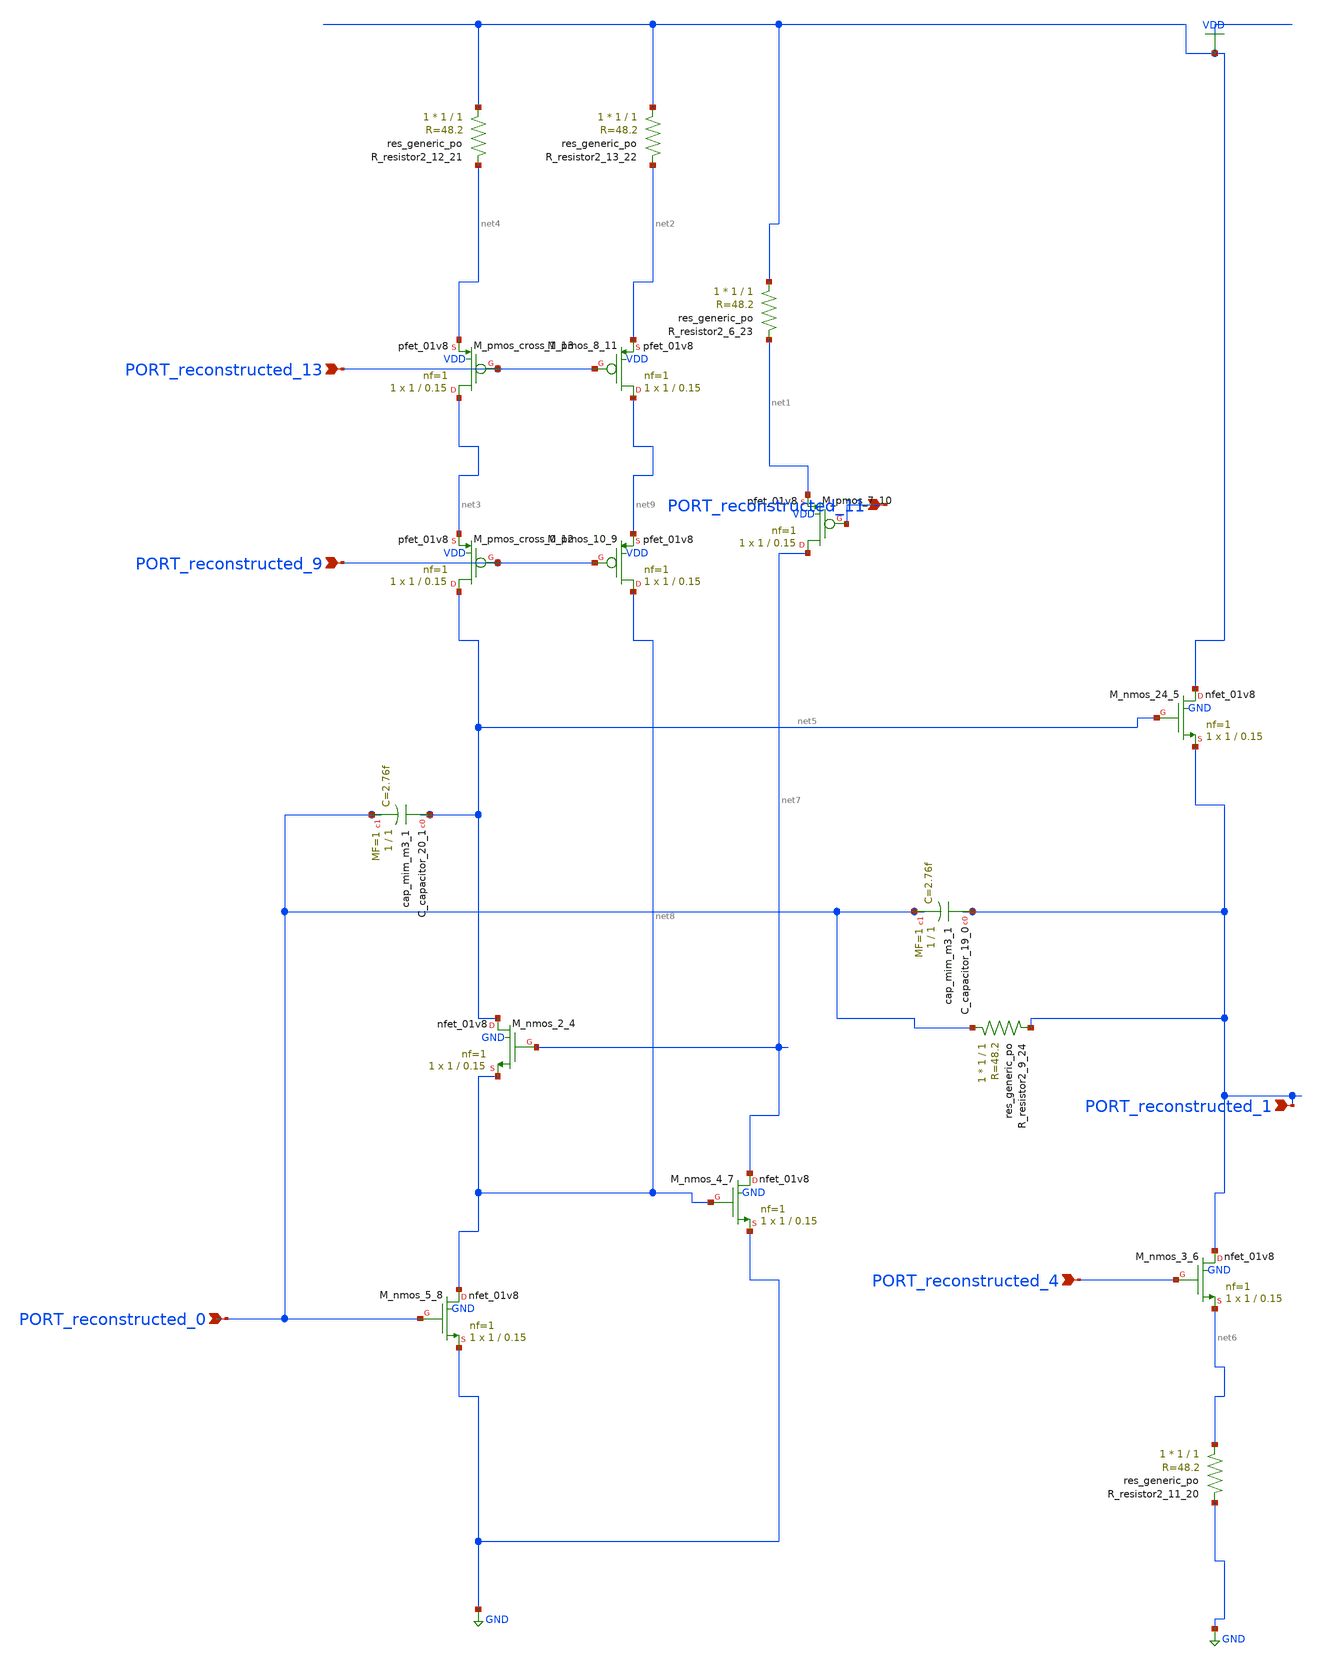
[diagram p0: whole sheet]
** sch_path: schematics/10_1016_j_nima_2022_167570_08_001.sch
**.subckt 10_1016_j_nima_2022_167570_08_001 PORT_reconstructed_13 PORT_reconstructed_4
*+ PORT_reconstructed_9 PORT_reconstructed_11 PORT_reconstructed_0 PORT_reconstructed_1
*.ipin PORT_reconstructed_13
*.ipin PORT_reconstructed_4
*.ipin PORT_reconstructed_9
*.ipin PORT_reconstructed_11
*.ipin PORT_reconstructed_0
*.ipin PORT_reconstructed_1
XC_capacitor_19_0 PORT_reconstructed_1 PORT_reconstructed_0 sky130_fd_pr__cap_mim_m3_1 W=1 L=1 MF=1
+ m=1
XC_capacitor_20_1 net5 PORT_reconstructed_0 sky130_fd_pr__cap_mim_m3_1 W=1 L=1 MF=1 m=1
XM_nmos_2_4 net5 net7 net8 GND sky130_fd_pr__nfet_01v8 L=0.15 W=1 nf=1 ad='int((1 + 1)/2) * 1 / 1 * 0.29'
+ as='int((1 + 2)/2) * 1 / 1 * 0.29' pd='2*int((1 + 1)/2) * (1 / 1 + 0.29)' ps='2*int((1 + 2)/2) * (1 / 1 + 0.29)'
+ nrd='0.29 / 1 ' nrs='0.29 / 1 ' sa=0 sb=0 sd=0 mult=1 m=1
XM_nmos_24_5 VDD net5 PORT_reconstructed_1 GND sky130_fd_pr__nfet_01v8 L=0.15 W=1 nf=1 ad='int((1 + 1)/2) * 1 / 1 * 0.29'
+ as='int((1 + 2)/2) * 1 / 1 * 0.29' pd='2*int((1 + 1)/2) * (1 / 1 + 0.29)' ps='2*int((1 + 2)/2) * (1 / 1 + 0.29)'
+ nrd='0.29 / 1 ' nrs='0.29 / 1 ' sa=0 sb=0 sd=0 mult=1 m=1
XM_nmos_3_6 PORT_reconstructed_1 PORT_reconstructed_4 net6 GND sky130_fd_pr__nfet_01v8 L=0.15 W=1 nf=1
+ ad='int((1 + 1)/2) * 1 / 1 * 0.29' as='int((1 + 2)/2) * 1 / 1 * 0.29' pd='2*int((1 + 1)/2) * (1 / 1 + 0.29)'
+ ps='2*int((1 + 2)/2) * (1 / 1 + 0.29)' nrd='0.29 / 1 ' nrs='0.29 / 1 ' sa=0 sb=0 sd=0 mult=1 m=1
XM_nmos_4_7 net7 net8 GND GND sky130_fd_pr__nfet_01v8 L=0.15 W=1 nf=1 ad='int((1 + 1)/2) * 1 / 1 * 0.29'
+ as='int((1 + 2)/2) * 1 / 1 * 0.29' pd='2*int((1 + 1)/2) * (1 / 1 + 0.29)' ps='2*int((1 + 2)/2) * (1 / 1 + 0.29)'
+ nrd='0.29 / 1 ' nrs='0.29 / 1 ' sa=0 sb=0 sd=0 mult=1 m=1
XM_nmos_5_8 net8 PORT_reconstructed_0 GND GND sky130_fd_pr__nfet_01v8 L=0.15 W=1 nf=1 ad='int((1 + 1)/2) * 1 / 1 * 0.29'
+ as='int((1 + 2)/2) * 1 / 1 * 0.29' pd='2*int((1 + 1)/2) * (1 / 1 + 0.29)' ps='2*int((1 + 2)/2) * (1 / 1 + 0.29)'
+ nrd='0.29 / 1 ' nrs='0.29 / 1 ' sa=0 sb=0 sd=0 mult=1 m=1
XM_pmos_10_9 net8 PORT_reconstructed_9 net9 VDD sky130_fd_pr__pfet_01v8 L=0.15 W=1 nf=1 ad='int((1 + 1)/2) * 1 / 1 * 0.29'
+ as='int((1 + 2)/2) * 1 / 1 * 0.29' pd='2*int((1 + 1)/2) * (1 / 1 + 0.29)' ps='2*int((1 + 2)/2) * (1 / 1 + 0.29)'
+ nrd='0.29 / 1 ' nrs='0.29 / 1 ' sa=0 sb=0 sd=0 mult=1 m=1
XM_pmos_7_10 net7 PORT_reconstructed_11 net1 VDD sky130_fd_pr__pfet_01v8 L=0.15 W=1 nf=1 ad='int((1 + 1)/2) * 1 / 1 * 0.29'
+ as='int((1 + 2)/2) * 1 / 1 * 0.29' pd='2*int((1 + 1)/2) * (1 / 1 + 0.29)' ps='2*int((1 + 2)/2) * (1 / 1 + 0.29)'
+ nrd='0.29 / 1 ' nrs='0.29 / 1 ' sa=0 sb=0 sd=0 mult=1 m=1
XM_pmos_8_11 net9 PORT_reconstructed_13 net2 VDD sky130_fd_pr__pfet_01v8 L=0.15 W=1 nf=1 ad='int((1 + 1)/2) * 1 / 1 * 0.29'
+ as='int((1 + 2)/2) * 1 / 1 * 0.29' pd='2*int((1 + 1)/2) * (1 / 1 + 0.29)' ps='2*int((1 + 2)/2) * (1 / 1 + 0.29)'
+ nrd='0.29 / 1 ' nrs='0.29 / 1 ' sa=0 sb=0 sd=0 mult=1 m=1
XM_pmos_cross_0_12 net5 PORT_reconstructed_9 net3 VDD sky130_fd_pr__pfet_01v8 L=0.15 W=1 nf=1 ad='int((1 + 1)/2) * 1 / 1 * 0.29'
+ as='int((1 + 2)/2) * 1 / 1 * 0.29' pd='2*int((1 + 1)/2) * (1 / 1 + 0.29)' ps='2*int((1 + 2)/2) * (1 / 1 + 0.29)'
+ nrd='0.29 / 1 ' nrs='0.29 / 1 ' sa=0 sb=0 sd=0 mult=1 m=1
XM_pmos_cross_1_13 net3 PORT_reconstructed_13 net4 VDD sky130_fd_pr__pfet_01v8 L=0.15 W=1 nf=1 ad='int((1 + 1)/2) * 1 / 1 * 0.29'
+ as='int((1 + 2)/2) * 1 / 1 * 0.29' pd='2*int((1 + 1)/2) * (1 / 1 + 0.29)' ps='2*int((1 + 2)/2) * (1 / 1 + 0.29)'
+ nrd='0.29 / 1 ' nrs='0.29 / 1 ' sa=0 sb=0 sd=0 mult=1 m=1
XR_resistor2_11_20 net6 GND sky130_fd_pr__res_generic_po W=1 L=1 m=1
XR_resistor2_12_21 VDD net4 sky130_fd_pr__res_generic_po W=1 L=1 m=1
XR_resistor2_13_22 VDD net2 sky130_fd_pr__res_generic_po W=1 L=1 m=1
XR_resistor2_6_23 VDD net1 sky130_fd_pr__res_generic_po W=1 L=1 m=1
XR_resistor2_9_24 PORT_reconstructed_0 PORT_reconstructed_1 sky130_fd_pr__res_generic_po W=1 L=1 m=1
**.ends
.GLOBAL GND
.GLOBAL VDD
.end
